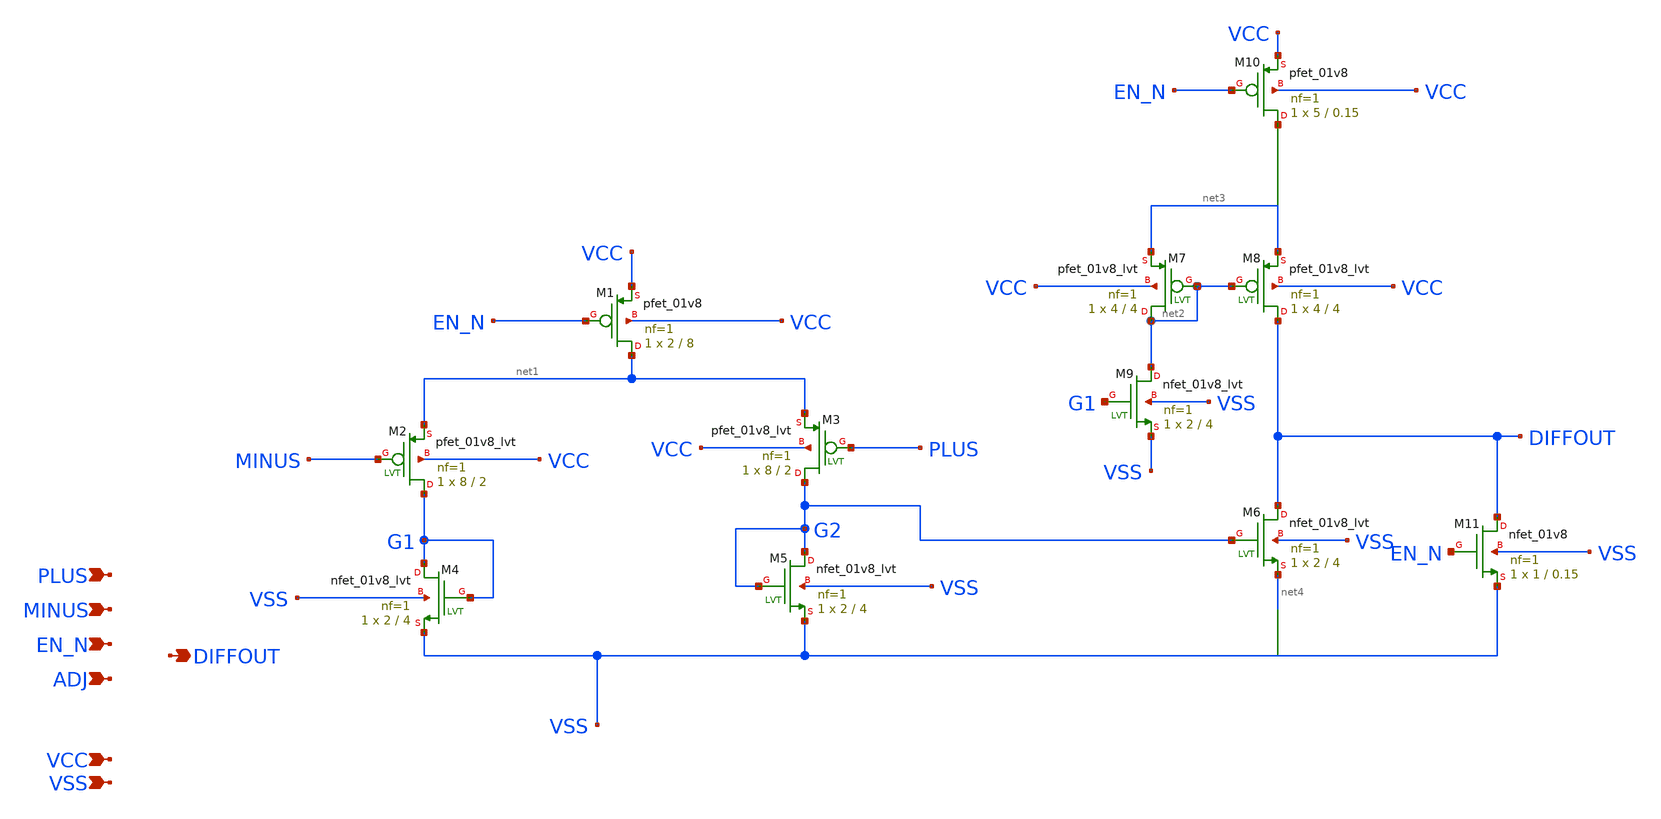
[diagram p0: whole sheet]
** sch_path: tuto1.sch
**.subckt tuto1 PLUS MINUS VCC VSS EN_N ADJ DIFFOUT
*.ipin PLUS
*.ipin MINUS
*.ipin VCC
*.ipin VSS
*.ipin EN_N
*.ipin ADJ
*.opin DIFFOUT
XM1 net1 EN_N VCC VCC sky130_fd_pr__pfet_01v8 L=8 W=2 nf=1 ad='int((1 + 1)/2) * 2 / 1 * 0.29' as='int((1 + 2)/2) * 2 / 1 * 0.29'
+ pd='2*int((1 + 1)/2) * (2 / 1 + 0.29)' ps='2*int((1 + 2)/2) * (2 / 1 + 0.29)' nrd='0.29 / 2 ' nrs='0.29 / 2 '
+ sa=0 sb=0 sd=0 mult=1 m=1
XM2 G1 MINUS net1 VCC sky130_fd_pr__pfet_01v8_lvt L=2 W=8 nf=1 ad='int((1 + 1)/2) * 8 / 1 * 0.29' as='int((1 + 2)/2) * 8 / 1 * 0.29'
+ pd='2*int((1 + 1)/2) * (8 / 1 + 0.29)' ps='2*int((1 + 2)/2) * (8 / 1 + 0.29)' nrd='0.29 / 8 ' nrs='0.29 / 8 '
+ sa=0 sb=0 sd=0 mult=1 m=1
XM3 G2 PLUS net1 VCC sky130_fd_pr__pfet_01v8_lvt L=2 W=8 nf=1 ad='int((1 + 1)/2) * 8 / 1 * 0.29' as='int((1 + 2)/2) * 8 / 1 * 0.29'
+ pd='2*int((1 + 1)/2) * (8 / 1 + 0.29)' ps='2*int((1 + 2)/2) * (8 / 1 + 0.29)' nrd='0.29 / 8 ' nrs='0.29 / 8 '
+ sa=0 sb=0 sd=0 mult=1 m=1
XM4 G1 G1 VSS VSS sky130_fd_pr__nfet_01v8_lvt L=4 W=2 nf=1 ad='int((1 + 1)/2) * 2 / 1 * 0.29' as='int((1 + 2)/2) * 2 / 1 * 0.29'
+ pd='2*int((1 + 1)/2) * (2 / 1 + 0.29)' ps='2*int((1 + 2)/2) * (2 / 1 + 0.29)' nrd='0.29 / 2 ' nrs='0.29 / 2 '
+ sa=0 sb=0 sd=0 mult=1 m=1
XM5 G2 G2 VSS VSS sky130_fd_pr__nfet_01v8_lvt L=4 W=2 nf=1 ad='int((1 + 1)/2) * 2 / 1 * 0.29' as='int((1 + 2)/2) * 2 / 1 * 0.29'
+ pd='2*int((1 + 1)/2) * (2 / 1 + 0.29)' ps='2*int((1 + 2)/2) * (2 / 1 + 0.29)' nrd='0.29 / 2 ' nrs='0.29 / 2 '
+ sa=0 sb=0 sd=0 mult=1 m=1
XM7 net2 net2 net3 VCC sky130_fd_pr__pfet_01v8_lvt L=4 W=4 nf=1 ad='int((1 + 1)/2) * 4 / 1 * 0.29' as='int((1 + 2)/2) * 4 / 1 * 0.29'
+ pd='2*int((1 + 1)/2) * (4 / 1 + 0.29)' ps='2*int((1 + 2)/2) * (4 / 1 + 0.29)' nrd='0.29 / 4 ' nrs='0.29 / 4 '
+ sa=0 sb=0 sd=0 mult=1 m=1
XM8 DIFFOUT net2 net3 VCC sky130_fd_pr__pfet_01v8_lvt L=4 W=4 nf=1 ad='int((1 + 1)/2) * 4 / 1 * 0.29'
+ as='int((1 + 2)/2) * 4 / 1 * 0.29' pd='2*int((1 + 1)/2) * (4 / 1 + 0.29)' ps='2*int((1 + 2)/2) * (4 / 1 + 0.29)'
+ nrd='0.29 / 4 ' nrs='0.29 / 4 ' sa=0 sb=0 sd=0 mult=1 m=1
XM9 net2 G1 VSS VSS sky130_fd_pr__nfet_01v8_lvt L=4 W=2 nf=1 ad='int((1 + 1)/2) * 2 / 1 * 0.29' as='int((1 + 2)/2) * 2 / 1 * 0.29'
+ pd='2*int((1 + 1)/2) * (2 / 1 + 0.29)' ps='2*int((1 + 2)/2) * (2 / 1 + 0.29)' nrd='0.29 / 2 ' nrs='0.29 / 2 '
+ sa=0 sb=0 sd=0 mult=1 m=1
XM10 net5 EN_N VCC VCC sky130_fd_pr__pfet_01v8 L=0.15 W=5 nf=1 ad='int((1 + 1)/2) * 5 / 1 * 0.29' as='int((1 + 2)/2) * 5 / 1 * 0.29'
+ pd='2*int((1 + 1)/2) * (5 / 1 + 0.29)' ps='2*int((1 + 2)/2) * (5 / 1 + 0.29)' nrd='0.29 / 5 ' nrs='0.29 / 5 '
+ sa=0 sb=0 sd=0 mult=1 m=1
XM11 DIFFOUT EN_N VSS VSS sky130_fd_pr__nfet_01v8 L=0.15 W=1 nf=1 ad='int((1 + 1)/2) * 1 / 1 * 0.29'
+ as='int((1 + 2)/2) * 1 / 1 * 0.29' pd='2*int((1 + 1)/2) * (1 / 1 + 0.29)' ps='2*int((1 + 2)/2) * (1 / 1 + 0.29)'
+ nrd='0.29 / 1 ' nrs='0.29 / 1 ' sa=0 sb=0 sd=0 mult=1 m=1
XM6 DIFFOUT G2 net4 VSS sky130_fd_pr__nfet_01v8_lvt L=4 W=2 nf=1 ad='int((1 + 1)/2) * 2 / 1 * 0.29' as='int((1 + 2)/2) * 2 / 1 * 0.29'
+ pd='2*int((1 + 1)/2) * (2 / 1 + 0.29)' ps='2*int((1 + 2)/2) * (2 / 1 + 0.29)' nrd='0.29 / 2 ' nrs='0.29 / 2 '
+ sa=0 sb=0 sd=0 mult=1 m=1
**.ends
.end
